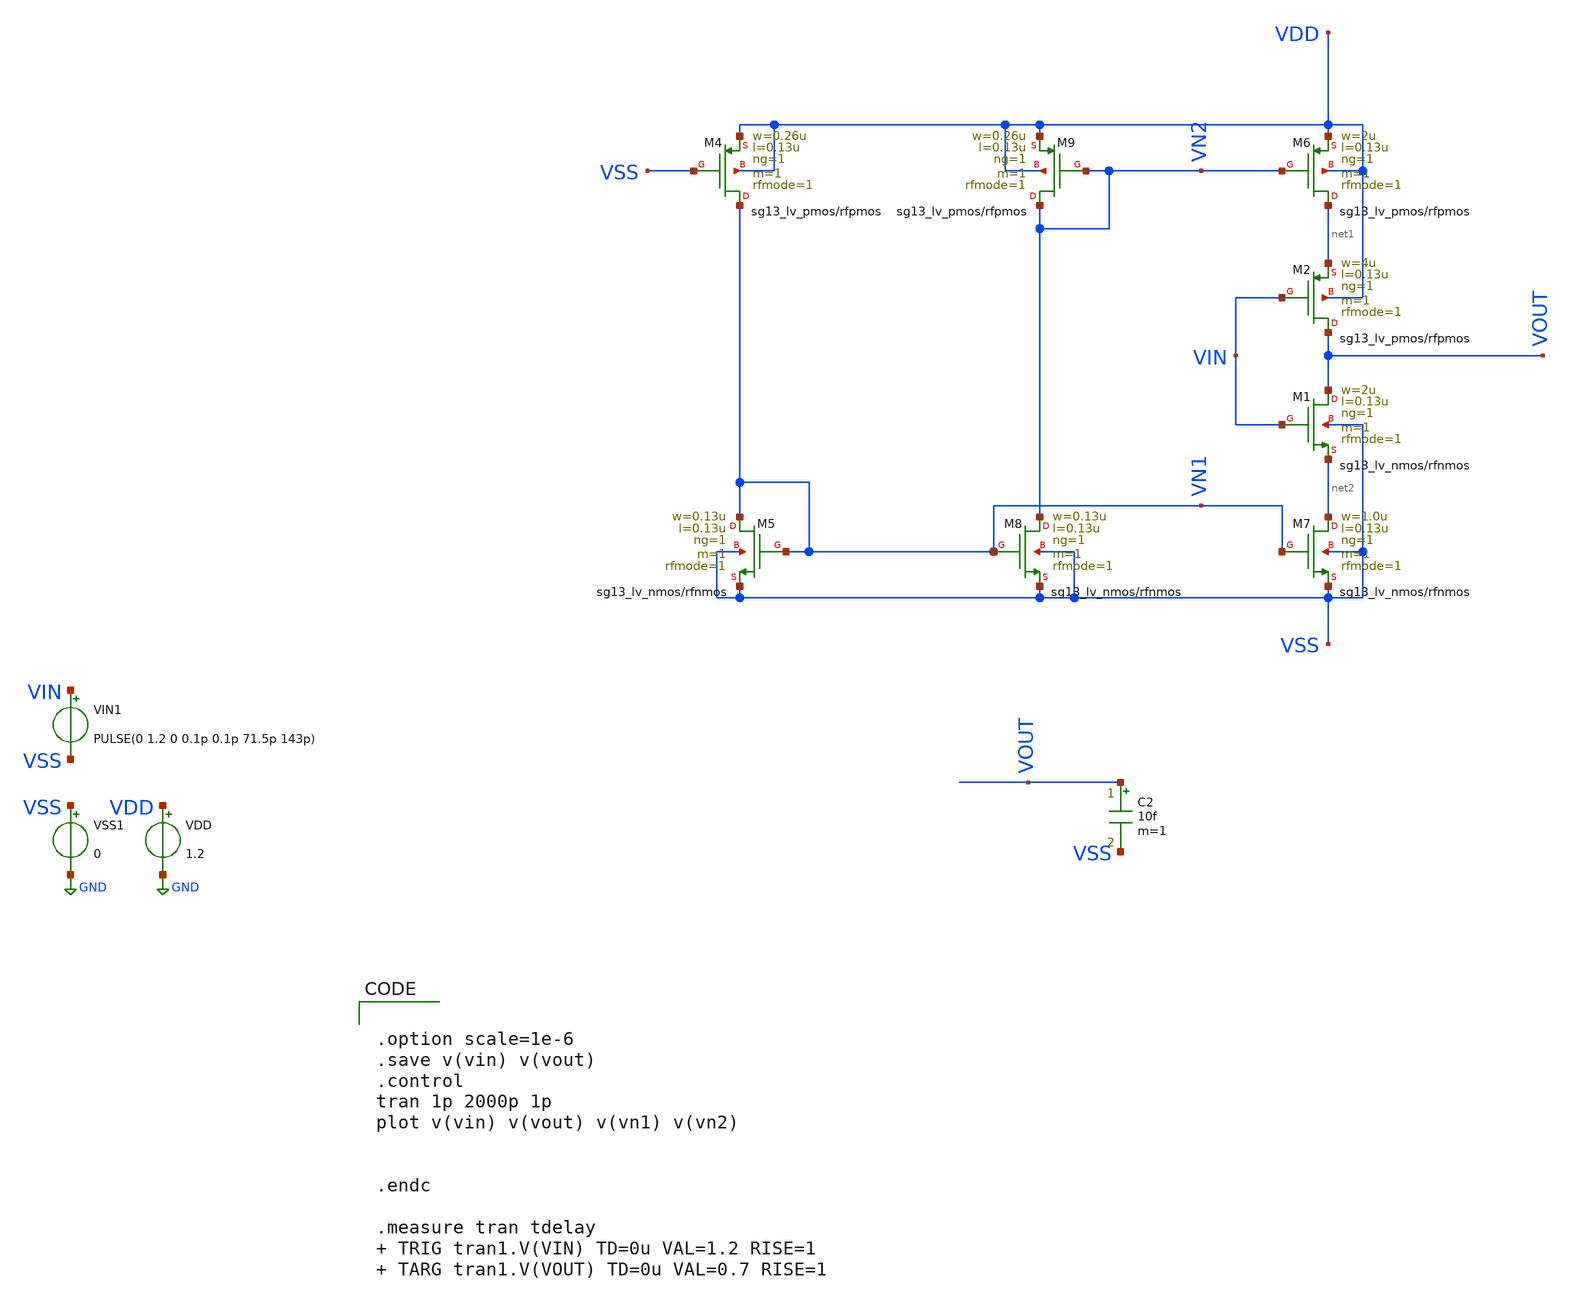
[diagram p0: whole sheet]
** sch_path: tb_delay_line_cdr.sch
**.subckt tb_delay_line_cdr
XM9 VN2 VN2 VDD VDD sg13_lv_pmos w=0.26u l=0.13u ng=1 m=1 rfmode=1 mm_ok=1
XM4 VN1 VSS VDD VDD sg13_lv_pmos w=0.26u l=0.13u ng=1 m=1 rfmode=1 mm_ok=1
XM6 net1 VN2 VDD VDD sg13_lv_pmos w=2u l=0.13u ng=1 m=1 rfmode=1 mm_ok=1
XM2 VOUT VIN net1 VDD sg13_lv_pmos w=4u l=0.13u ng=1 m=1 rfmode=1 mm_ok=1
XM5 VN1 VN1 VSS VSS sg13_lv_nmos w=0.13u l=0.13u ng=1 m=1 rfmode=1 mm_ok=1
XM8 VN2 VN1 VSS VSS sg13_lv_nmos w=0.13u l=0.13u ng=1 m=1 rfmode=1 mm_ok=1
XM7 net2 VN1 VSS VSS sg13_lv_nmos w=1.0u l=0.13u ng=1 m=1 rfmode=1 mm_ok=1
XM1 VOUT VIN net2 VSS sg13_lv_nmos w=2u l=0.13u ng=1 m=1 rfmode=1 mm_ok=1
VDD VDD GND 1.2
VSS1 VSS GND 0
VIN1 VIN VSS PULSE(0 1.2 0 0.1p 0.1p 71.5p 143p)
C2 VOUT VSS 10f m=1
**** begin user architecture code


.option scale=1e-6
.save v(vin) v(vout)
.control
tran 1p 2000p 1p
plot v(vin) v(vout) v(vn1) v(vn2)


.endc

.measure tran tdelay  TRIG tran1.V(VIN) TD=0u VAL=1.2 RISE=1  TARG tran1.V(VOUT) TD=0u VAL=0.7
+ RISE=1






.param corner=0

.if (corner==0)
.lib $::SG13G2_MODELS/cornerMOSlv.lib mos_tt
.lib $::SG13G2_MODELS/cornerMOSlv.lib mos_tt
.lib $::SG13G2_MODELS/cornerRES.lib res_typ
.lib $::SG13G2_MODELS/cornerCAP.lib cap_typ
.endif

.include /opt/pdks/ihp-sg13g2/libs.ref/sg13g2_stdcell/spice/sg13g2_stdcell.spice

**** end user architecture code
**.ends
.GLOBAL GND
.end
